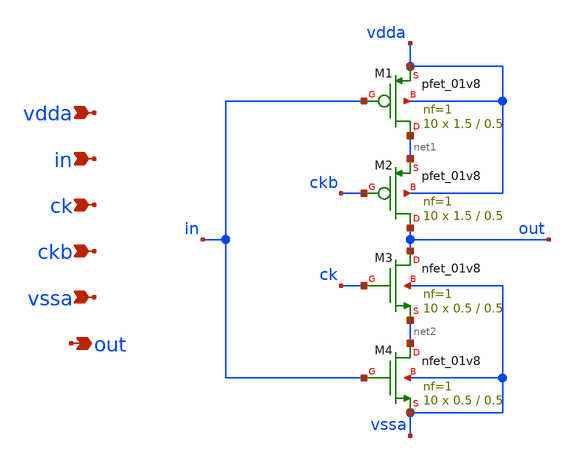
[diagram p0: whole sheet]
** sch_path: xschem/dac_sw_6.sch
**.subckt dac_sw_6 vdda in ck ckb vssa out
*.ipin vdda
*.ipin in
*.ipin ck
*.ipin ckb
*.ipin vssa
*.opin out
XM1 net1 in vdda vdda sky130_fd_pr__pfet_01v8 L=0.5 W=1.5 nf=1 ad='int((nf+1)/2) * W/nf * 0.29' as='int((nf+2)/2) * W/nf * 0.29'
+ pd='2*int((nf+1)/2) * (W/nf + 0.29)' ps='2*int((nf+2)/2) * (W/nf + 0.29)' nrd='0.29 / W' nrs='0.29 / W'
+ sa=0 sb=0 sd=0 mult=10 m=10
XM2 out ckb net1 vdda sky130_fd_pr__pfet_01v8 L=0.5 W=1.5 nf=1 ad='int((nf+1)/2) * W/nf * 0.29' as='int((nf+2)/2) * W/nf * 0.29'
+ pd='2*int((nf+1)/2) * (W/nf + 0.29)' ps='2*int((nf+2)/2) * (W/nf + 0.29)' nrd='0.29 / W' nrs='0.29 / W'
+ sa=0 sb=0 sd=0 mult=10 m=10
XM3 out ck net2 vssa sky130_fd_pr__nfet_01v8 L=0.5 W=0.5 nf=1 ad='int((nf+1)/2) * W/nf * 0.29' as='int((nf+2)/2) * W/nf * 0.29'
+ pd='2*int((nf+1)/2) * (W/nf + 0.29)' ps='2*int((nf+2)/2) * (W/nf + 0.29)' nrd='0.29 / W' nrs='0.29 / W'
+ sa=0 sb=0 sd=0 mult=10 m=10
XM4 net2 in vssa vssa sky130_fd_pr__nfet_01v8 L=0.5 W=0.5 nf=1 ad='int((nf+1)/2) * W/nf * 0.29' as='int((nf+2)/2) * W/nf * 0.29'
+ pd='2*int((nf+1)/2) * (W/nf + 0.29)' ps='2*int((nf+2)/2) * (W/nf + 0.29)' nrd='0.29 / W' nrs='0.29 / W'
+ sa=0 sb=0 sd=0 mult=10 m=10
**.ends
.end
